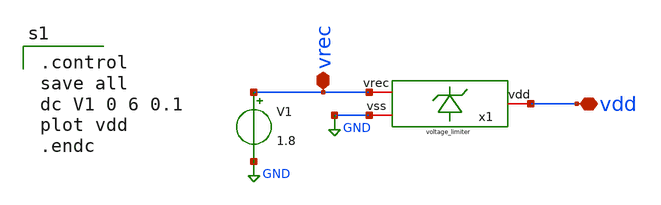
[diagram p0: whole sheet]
** sch_path: XSCHEM/voltage_limiter_tb.sch
**.subckt voltage_limiter_tb vdd vrec
*.iopin vdd
*.iopin vrec
V1 vrec GND 1.8
x1 vrec vdd GND voltage_limiter
**** begin user architecture code

.control
save all
dc V1 0 6 0.1
plot vdd
.endc


** opencircuitdesign pdks install
.lib $::SKYWATER_MODELS/sky130.lib.spice tt


**** end user architecture code
**.ends

* expanding   symbol:  Documentos/TESIS DE GRADO/WORK_IN_PROGRESS/My_xschem/voltage_limiter.sym # of
*+ pins=3
** sym_path: XSCHEM/voltage_limiter.sym
** sch_path: XSCHEM/voltage_limiter.sch
.subckt voltage_limiter vrec vdd vss
*.iopin vss
*.iopin vrec
*.iopin vdd
XM4 net1 net4 vss vss sky130_fd_pr__nfet_01v8_lvt L=0.7 W=2 nf=1 ad='int((nf+1)/2) * W/nf * 0.29' as='int((nf+2)/2) * W/nf * 0.29'
+ pd='2*int((nf+1)/2) * (W/nf + 0.29)' ps='2*int((nf+2)/2) * (W/nf + 0.29)' nrd='0.29 / W' nrs='0.29 / W'
+ sa=0 sb=0 sd=0 mult=1 m=1
XM5 vss net1 vdd vdd sky130_fd_pr__pfet_01v8_lvt L=0.35 W=16 nf=4 ad='int((nf+1)/2) * W/nf * 0.29' as='int((nf+2)/2) * W/nf * 0.29'
+ pd='2*int((nf+1)/2) * (W/nf + 0.29)' ps='2*int((nf+2)/2) * (W/nf + 0.29)' nrd='0.29 / W' nrs='0.29 / W'
+ sa=0 sb=0 sd=0 mult=1 m=1
XM1 net2 net2 vdd vdd sky130_fd_pr__pfet_01v8_lvt L=0.35 W=4 nf=1 ad='int((nf+1)/2) * W/nf * 0.29' as='int((nf+2)/2) * W/nf * 0.29'
+ pd='2*int((nf+1)/2) * (W/nf + 0.29)' ps='2*int((nf+2)/2) * (W/nf + 0.29)' nrd='0.29 / W' nrs='0.29 / W'
+ sa=0 sb=0 sd=0 mult=2 m=2
XM2 net3 net3 net2 vdd sky130_fd_pr__pfet_01v8_lvt L=0.35 W=4 nf=1 ad='int((nf+1)/2) * W/nf * 0.29' as='int((nf+2)/2) * W/nf * 0.29'
+ pd='2*int((nf+1)/2) * (W/nf + 0.29)' ps='2*int((nf+2)/2) * (W/nf + 0.29)' nrd='0.29 / W' nrs='0.29 / W'
+ sa=0 sb=0 sd=0 mult=2 m=2
XM3 net4 net4 net3 vdd sky130_fd_pr__pfet_01v8_lvt L=0.35 W=4 nf=1 ad='int((nf+1)/2) * W/nf * 0.29' as='int((nf+2)/2) * W/nf * 0.29'
+ pd='2*int((nf+1)/2) * (W/nf + 0.29)' ps='2*int((nf+2)/2) * (W/nf + 0.29)' nrd='0.29 / W' nrs='0.29 / W'
+ sa=0 sb=0 sd=0 mult=2 m=2
XR2 net1 vdd vss sky130_fd_pr__res_xhigh_po W=1 L=60 mult=1 m=1
XR4 vss net4 vss sky130_fd_pr__res_xhigh_po W=1 L=40 mult=1 m=1
R1 vdd vrec sky130_fd_pr__res_generic_l1 W=1 L=18 m=1
.ends

.GLOBAL GND
.end
